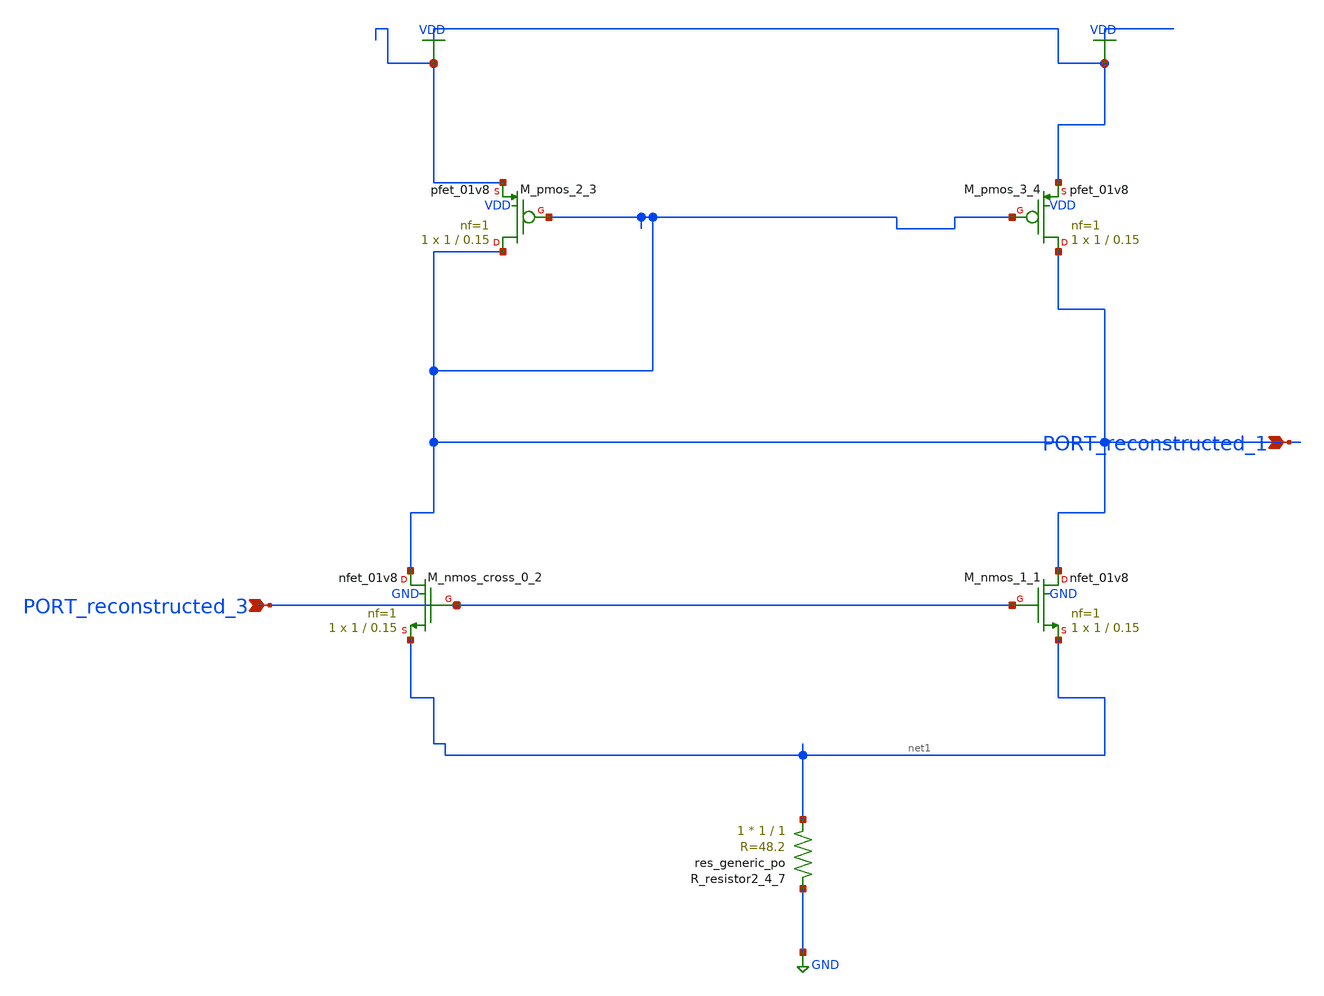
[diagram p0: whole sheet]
** sch_path: schematics/AMSNet/288.sch
**.subckt 288 PORT_reconstructed_3 PORT_reconstructed_1
*.ipin PORT_reconstructed_3
*.ipin PORT_reconstructed_1
XM_nmos_1_1 PORT_reconstructed_1 PORT_reconstructed_3 net1 GND sky130_fd_pr__nfet_01v8 L=0.15 W=1 nf=1
+ ad='int((1 + 1)/2) * 1 / 1 * 0.29' as='int((1 + 2)/2) * 1 / 1 * 0.29' pd='2*int((1 + 1)/2) * (1 / 1 + 0.29)'
+ ps='2*int((1 + 2)/2) * (1 / 1 + 0.29)' nrd='0.29 / 1 ' nrs='0.29 / 1 ' sa=0 sb=0 sd=0 mult=1 m=1
XM_nmos_cross_0_2 PORT_reconstructed_1 PORT_reconstructed_3 net1 GND sky130_fd_pr__nfet_01v8 L=0.15 W=1
+ nf=1 ad='int((1 + 1)/2) * 1 / 1 * 0.29' as='int((1 + 2)/2) * 1 / 1 * 0.29' pd='2*int((1 + 1)/2) * (1 / 1 + 0.29)'
+ ps='2*int((1 + 2)/2) * (1 / 1 + 0.29)' nrd='0.29 / 1 ' nrs='0.29 / 1 ' sa=0 sb=0 sd=0 mult=1 m=1
XM_pmos_2_3 PORT_reconstructed_1 PORT_reconstructed_1 VDD VDD sky130_fd_pr__pfet_01v8 L=0.15 W=1 nf=1
+ ad='int((1 + 1)/2) * 1 / 1 * 0.29' as='int((1 + 2)/2) * 1 / 1 * 0.29' pd='2*int((1 + 1)/2) * (1 / 1 + 0.29)'
+ ps='2*int((1 + 2)/2) * (1 / 1 + 0.29)' nrd='0.29 / 1 ' nrs='0.29 / 1 ' sa=0 sb=0 sd=0 mult=1 m=1
XM_pmos_3_4 PORT_reconstructed_1 PORT_reconstructed_1 VDD VDD sky130_fd_pr__pfet_01v8 L=0.15 W=1 nf=1
+ ad='int((1 + 1)/2) * 1 / 1 * 0.29' as='int((1 + 2)/2) * 1 / 1 * 0.29' pd='2*int((1 + 1)/2) * (1 / 1 + 0.29)'
+ ps='2*int((1 + 2)/2) * (1 / 1 + 0.29)' nrd='0.29 / 1 ' nrs='0.29 / 1 ' sa=0 sb=0 sd=0 mult=1 m=1
XR_resistor2_4_7 net1 GND sky130_fd_pr__res_generic_po W=1 L=1 m=1
**.ends
.GLOBAL GND
.GLOBAL VDD
.end
